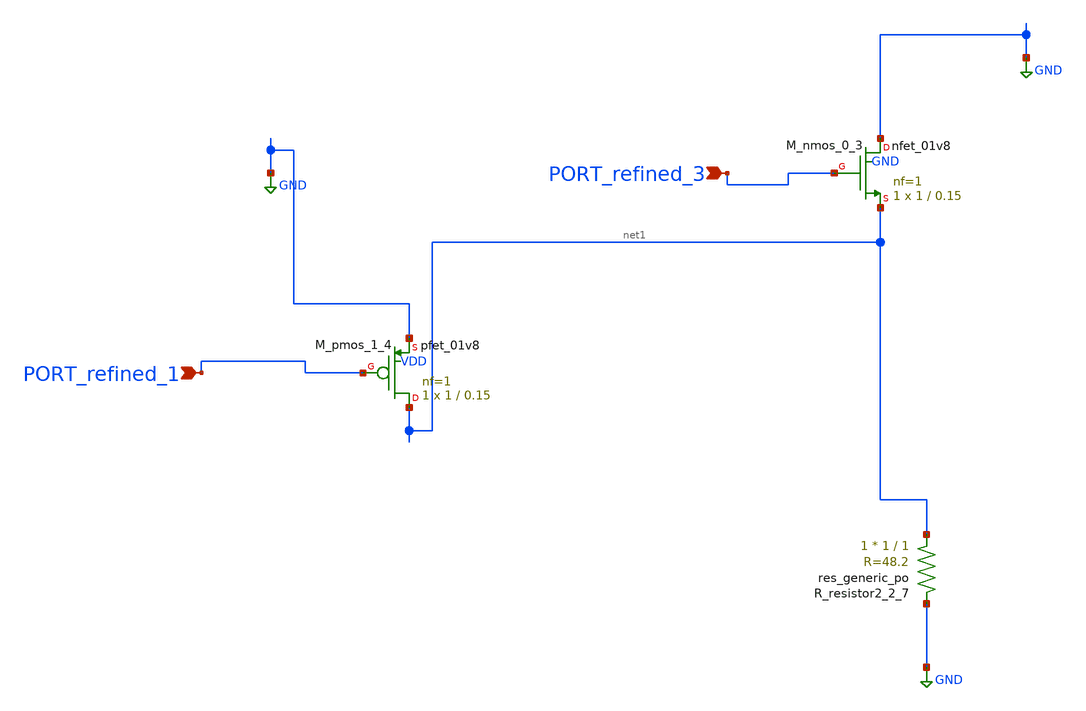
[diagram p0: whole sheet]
** sch_path: schematics/AMSNet/640.sch
**.subckt 640 PORT_refined_3 PORT_refined_1
*.ipin PORT_refined_3
*.ipin PORT_refined_1
XM_nmos_0_3 GND PORT_refined_3 net1 GND sky130_fd_pr__nfet_01v8 L=0.15 W=1 nf=1 ad='int((1 + 1)/2) * 1 / 1 * 0.29'
+ as='int((1 + 2)/2) * 1 / 1 * 0.29' pd='2*int((1 + 1)/2) * (1 / 1 + 0.29)' ps='2*int((1 + 2)/2) * (1 / 1 + 0.29)'
+ nrd='0.29 / 1 ' nrs='0.29 / 1 ' sa=0 sb=0 sd=0 mult=1 m=1
XM_pmos_1_4 net1 PORT_refined_1 GND VDD sky130_fd_pr__pfet_01v8 L=0.15 W=1 nf=1 ad='int((1 + 1)/2) * 1 / 1 * 0.29'
+ as='int((1 + 2)/2) * 1 / 1 * 0.29' pd='2*int((1 + 1)/2) * (1 / 1 + 0.29)' ps='2*int((1 + 2)/2) * (1 / 1 + 0.29)'
+ nrd='0.29 / 1 ' nrs='0.29 / 1 ' sa=0 sb=0 sd=0 mult=1 m=1
XR_resistor2_2_7 net1 GND sky130_fd_pr__res_generic_po W=1 L=1 m=1
**.ends
.GLOBAL GND
.end
